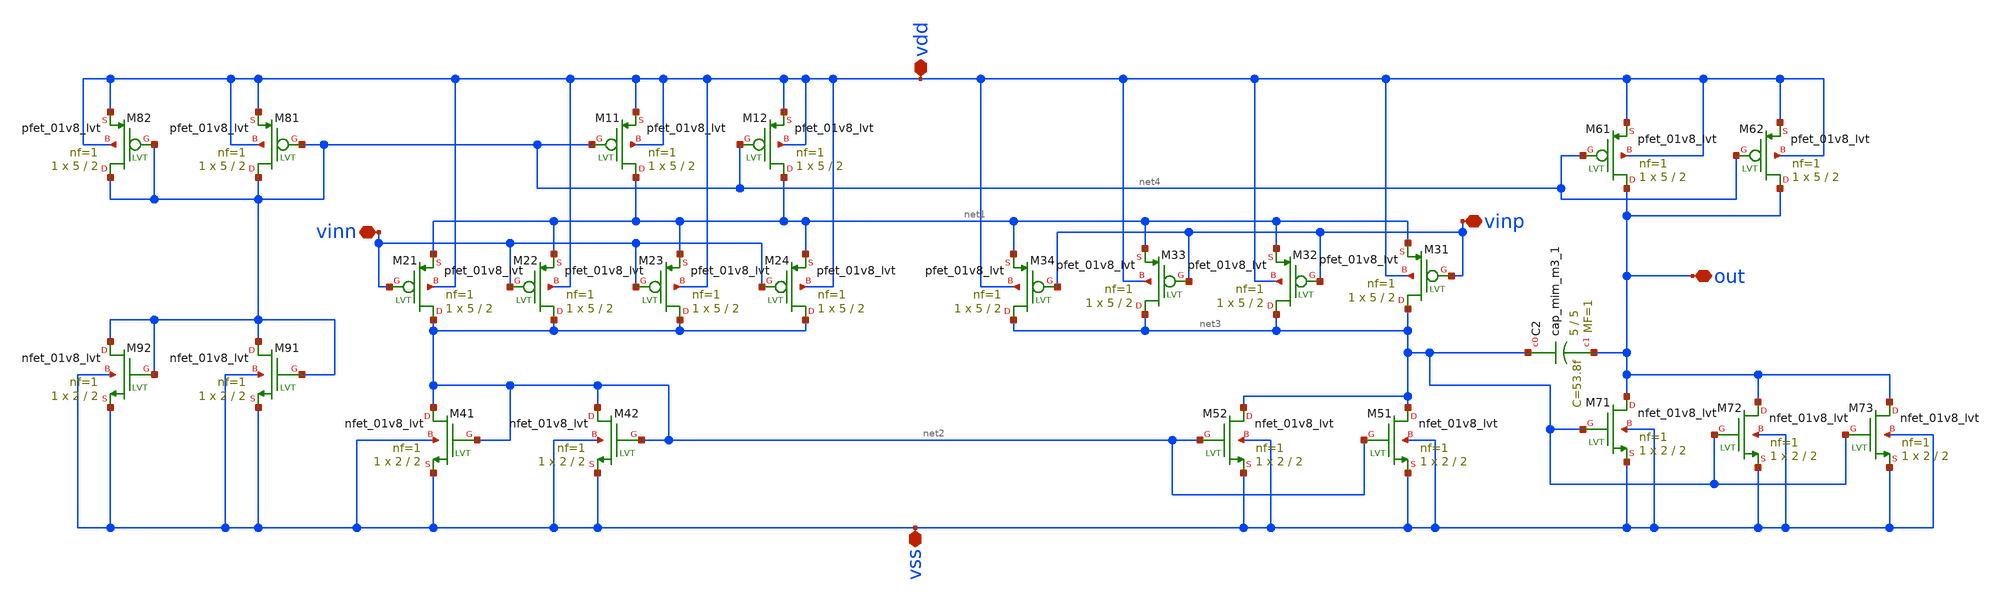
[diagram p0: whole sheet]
** sch_path: XSCHEM/For_Layout/OPAMP_lvt_PMOS.sch
**.subckt OPAMP_lvt_PMOS vdd vss out vinp vinn
*.iopin vdd
*.iopin vss
*.iopin out
*.iopin vinp
*.iopin vinn
XC2 net3 out sky130_fd_pr__cap_mim_m3_1 W=5 L=5 MF=1 m=1
XM11 net1 net4 vdd vdd sky130_fd_pr__pfet_01v8_lvt L=2 W=5 nf=1 ad='int((nf+1)/2) * W/nf * 0.29' as='int((nf+2)/2) * W/nf * 0.29'
+ pd='2*int((nf+1)/2) * (W/nf + 0.29)' ps='2*int((nf+2)/2) * (W/nf + 0.29)' nrd='0.29 / W' nrs='0.29 / W'
+ sa=0 sb=0 sd=0 mult=1 m=1
XM21 net2 vinn net1 vdd sky130_fd_pr__pfet_01v8_lvt L=2 W=5 nf=1 ad='int((nf+1)/2) * W/nf * 0.29' as='int((nf+2)/2) * W/nf * 0.29'
+ pd='2*int((nf+1)/2) * (W/nf + 0.29)' ps='2*int((nf+2)/2) * (W/nf + 0.29)' nrd='0.29 / W' nrs='0.29 / W'
+ sa=0 sb=0 sd=0 mult=1 m=1
XM31 net3 vinp net1 vdd sky130_fd_pr__pfet_01v8_lvt L=2 W=5 nf=1 ad='int((nf+1)/2) * W/nf * 0.29' as='int((nf+2)/2) * W/nf * 0.29'
+ pd='2*int((nf+1)/2) * (W/nf + 0.29)' ps='2*int((nf+2)/2) * (W/nf + 0.29)' nrd='0.29 / W' nrs='0.29 / W'
+ sa=0 sb=0 sd=0 mult=1 m=1
XM41 net2 net2 vss vss sky130_fd_pr__nfet_01v8_lvt L=2 W=2 nf=1 ad='int((nf+1)/2) * W/nf * 0.29' as='int((nf+2)/2) * W/nf * 0.29'
+ pd='2*int((nf+1)/2) * (W/nf + 0.29)' ps='2*int((nf+2)/2) * (W/nf + 0.29)' nrd='0.29 / W' nrs='0.29 / W'
+ sa=0 sb=0 sd=0 mult=1 m=1
XM51 net3 net2 vss vss sky130_fd_pr__nfet_01v8_lvt L=2 W=2 nf=1 ad='int((nf+1)/2) * W/nf * 0.29' as='int((nf+2)/2) * W/nf * 0.29'
+ pd='2*int((nf+1)/2) * (W/nf + 0.29)' ps='2*int((nf+2)/2) * (W/nf + 0.29)' nrd='0.29 / W' nrs='0.29 / W'
+ sa=0 sb=0 sd=0 mult=1 m=1
XM61 out net4 vdd vdd sky130_fd_pr__pfet_01v8_lvt L=2 W=5 nf=1 ad='int((nf+1)/2) * W/nf * 0.29' as='int((nf+2)/2) * W/nf * 0.29'
+ pd='2*int((nf+1)/2) * (W/nf + 0.29)' ps='2*int((nf+2)/2) * (W/nf + 0.29)' nrd='0.29 / W' nrs='0.29 / W'
+ sa=0 sb=0 sd=0 mult=1 m=1
XM71 out net3 vss vss sky130_fd_pr__nfet_01v8_lvt L=2 W=2 nf=1 ad='int((nf+1)/2) * W/nf * 0.29' as='int((nf+2)/2) * W/nf * 0.29'
+ pd='2*int((nf+1)/2) * (W/nf + 0.29)' ps='2*int((nf+2)/2) * (W/nf + 0.29)' nrd='0.29 / W' nrs='0.29 / W'
+ sa=0 sb=0 sd=0 mult=1 m=1
XM81 net4 net4 vdd vdd sky130_fd_pr__pfet_01v8_lvt L=2 W=5 nf=1 ad='int((nf+1)/2) * W/nf * 0.29' as='int((nf+2)/2) * W/nf * 0.29'
+ pd='2*int((nf+1)/2) * (W/nf + 0.29)' ps='2*int((nf+2)/2) * (W/nf + 0.29)' nrd='0.29 / W' nrs='0.29 / W'
+ sa=0 sb=0 sd=0 mult=1 m=1
XM91 net4 net4 vss vss sky130_fd_pr__nfet_01v8_lvt L=2 W=2 nf=1 ad='int((nf+1)/2) * W/nf * 0.29' as='int((nf+2)/2) * W/nf * 0.29'
+ pd='2*int((nf+1)/2) * (W/nf + 0.29)' ps='2*int((nf+2)/2) * (W/nf + 0.29)' nrd='0.29 / W' nrs='0.29 / W'
+ sa=0 sb=0 sd=0 mult=1 m=1
XM92 net4 net4 vss vss sky130_fd_pr__nfet_01v8_lvt L=2 W=2 nf=1 ad='int((nf+1)/2) * W/nf * 0.29' as='int((nf+2)/2) * W/nf * 0.29'
+ pd='2*int((nf+1)/2) * (W/nf + 0.29)' ps='2*int((nf+2)/2) * (W/nf + 0.29)' nrd='0.29 / W' nrs='0.29 / W'
+ sa=0 sb=0 sd=0 mult=1 m=1
XM82 net4 net4 vdd vdd sky130_fd_pr__pfet_01v8_lvt L=2 W=5 nf=1 ad='int((nf+1)/2) * W/nf * 0.29' as='int((nf+2)/2) * W/nf * 0.29'
+ pd='2*int((nf+1)/2) * (W/nf + 0.29)' ps='2*int((nf+2)/2) * (W/nf + 0.29)' nrd='0.29 / W' nrs='0.29 / W'
+ sa=0 sb=0 sd=0 mult=1 m=1
XM12 net1 net4 vdd vdd sky130_fd_pr__pfet_01v8_lvt L=2 W=5 nf=1 ad='int((nf+1)/2) * W/nf * 0.29' as='int((nf+2)/2) * W/nf * 0.29'
+ pd='2*int((nf+1)/2) * (W/nf + 0.29)' ps='2*int((nf+2)/2) * (W/nf + 0.29)' nrd='0.29 / W' nrs='0.29 / W'
+ sa=0 sb=0 sd=0 mult=1 m=1
XM22 net2 vinn net1 vdd sky130_fd_pr__pfet_01v8_lvt L=2 W=5 nf=1 ad='int((nf+1)/2) * W/nf * 0.29' as='int((nf+2)/2) * W/nf * 0.29'
+ pd='2*int((nf+1)/2) * (W/nf + 0.29)' ps='2*int((nf+2)/2) * (W/nf + 0.29)' nrd='0.29 / W' nrs='0.29 / W'
+ sa=0 sb=0 sd=0 mult=1 m=1
XM23 net2 vinn net1 vdd sky130_fd_pr__pfet_01v8_lvt L=2 W=5 nf=1 ad='int((nf+1)/2) * W/nf * 0.29' as='int((nf+2)/2) * W/nf * 0.29'
+ pd='2*int((nf+1)/2) * (W/nf + 0.29)' ps='2*int((nf+2)/2) * (W/nf + 0.29)' nrd='0.29 / W' nrs='0.29 / W'
+ sa=0 sb=0 sd=0 mult=1 m=1
XM24 net2 vinn net1 vdd sky130_fd_pr__pfet_01v8_lvt L=2 W=5 nf=1 ad='int((nf+1)/2) * W/nf * 0.29' as='int((nf+2)/2) * W/nf * 0.29'
+ pd='2*int((nf+1)/2) * (W/nf + 0.29)' ps='2*int((nf+2)/2) * (W/nf + 0.29)' nrd='0.29 / W' nrs='0.29 / W'
+ sa=0 sb=0 sd=0 mult=1 m=1
XM42 net2 net2 vss vss sky130_fd_pr__nfet_01v8_lvt L=2 W=2 nf=1 ad='int((nf+1)/2) * W/nf * 0.29' as='int((nf+2)/2) * W/nf * 0.29'
+ pd='2*int((nf+1)/2) * (W/nf + 0.29)' ps='2*int((nf+2)/2) * (W/nf + 0.29)' nrd='0.29 / W' nrs='0.29 / W'
+ sa=0 sb=0 sd=0 mult=1 m=1
XM34 net3 vinp net1 vdd sky130_fd_pr__pfet_01v8_lvt L=2 W=5 nf=1 ad='int((nf+1)/2) * W/nf * 0.29' as='int((nf+2)/2) * W/nf * 0.29'
+ pd='2*int((nf+1)/2) * (W/nf + 0.29)' ps='2*int((nf+2)/2) * (W/nf + 0.29)' nrd='0.29 / W' nrs='0.29 / W'
+ sa=0 sb=0 sd=0 mult=1 m=1
XM33 net3 vinp net1 vdd sky130_fd_pr__pfet_01v8_lvt L=2 W=5 nf=1 ad='int((nf+1)/2) * W/nf * 0.29' as='int((nf+2)/2) * W/nf * 0.29'
+ pd='2*int((nf+1)/2) * (W/nf + 0.29)' ps='2*int((nf+2)/2) * (W/nf + 0.29)' nrd='0.29 / W' nrs='0.29 / W'
+ sa=0 sb=0 sd=0 mult=1 m=1
XM32 net3 vinp net1 vdd sky130_fd_pr__pfet_01v8_lvt L=2 W=5 nf=1 ad='int((nf+1)/2) * W/nf * 0.29' as='int((nf+2)/2) * W/nf * 0.29'
+ pd='2*int((nf+1)/2) * (W/nf + 0.29)' ps='2*int((nf+2)/2) * (W/nf + 0.29)' nrd='0.29 / W' nrs='0.29 / W'
+ sa=0 sb=0 sd=0 mult=1 m=1
XM52 net3 net2 vss vss sky130_fd_pr__nfet_01v8_lvt L=2 W=2 nf=1 ad='int((nf+1)/2) * W/nf * 0.29' as='int((nf+2)/2) * W/nf * 0.29'
+ pd='2*int((nf+1)/2) * (W/nf + 0.29)' ps='2*int((nf+2)/2) * (W/nf + 0.29)' nrd='0.29 / W' nrs='0.29 / W'
+ sa=0 sb=0 sd=0 mult=1 m=1
XM62 out net4 vdd vdd sky130_fd_pr__pfet_01v8_lvt L=2 W=5 nf=1 ad='int((nf+1)/2) * W/nf * 0.29' as='int((nf+2)/2) * W/nf * 0.29'
+ pd='2*int((nf+1)/2) * (W/nf + 0.29)' ps='2*int((nf+2)/2) * (W/nf + 0.29)' nrd='0.29 / W' nrs='0.29 / W'
+ sa=0 sb=0 sd=0 mult=1 m=1
XM72 out net3 vss vss sky130_fd_pr__nfet_01v8_lvt L=2 W=2 nf=1 ad='int((nf+1)/2) * W/nf * 0.29' as='int((nf+2)/2) * W/nf * 0.29'
+ pd='2*int((nf+1)/2) * (W/nf + 0.29)' ps='2*int((nf+2)/2) * (W/nf + 0.29)' nrd='0.29 / W' nrs='0.29 / W'
+ sa=0 sb=0 sd=0 mult=1 m=1
XM73 out net3 vss vss sky130_fd_pr__nfet_01v8_lvt L=2 W=2 nf=1 ad='int((nf+1)/2) * W/nf * 0.29' as='int((nf+2)/2) * W/nf * 0.29'
+ pd='2*int((nf+1)/2) * (W/nf + 0.29)' ps='2*int((nf+2)/2) * (W/nf + 0.29)' nrd='0.29 / W' nrs='0.29 / W'
+ sa=0 sb=0 sd=0 mult=1 m=1
**.ends
.end
